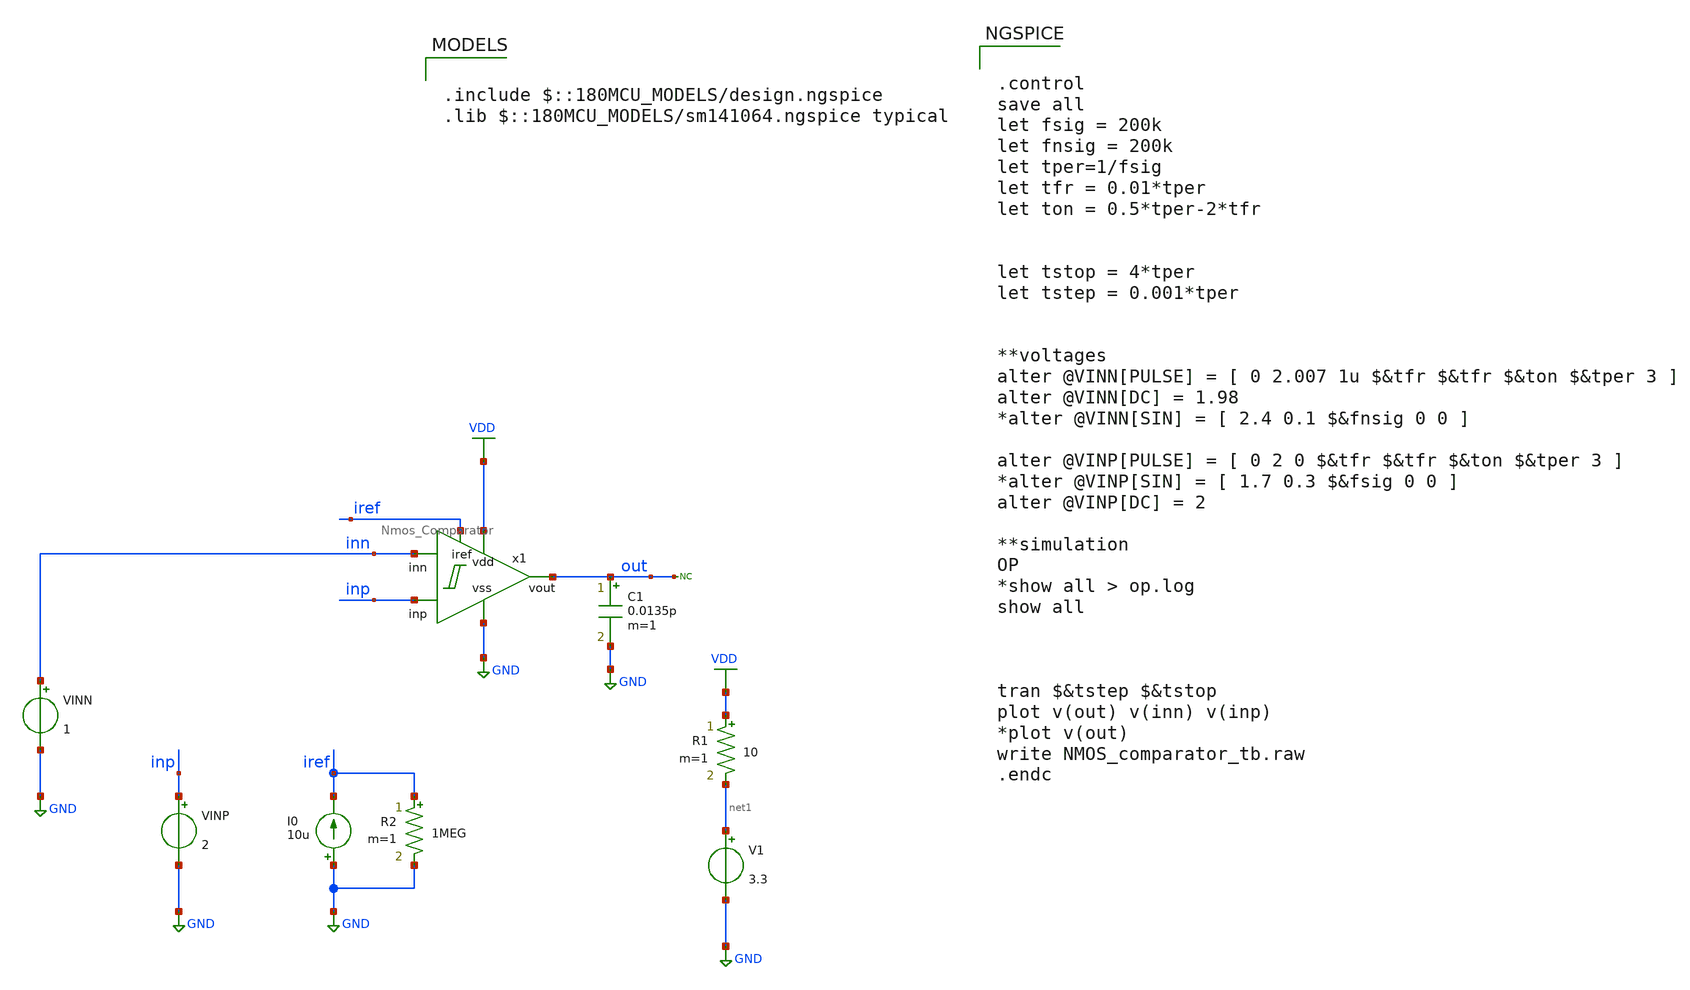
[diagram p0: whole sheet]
** sch_path: designs/libs/tb_analog/Comparator/NMOS_comparator_tb.sch
**.subckt NMOS_comparator_tb
I0 GND iref 10u
V1 net1 GND 3.3
VINP inp GND 2
* noconn out
VINN inn GND 1
x1 VDD out inp GND inn iref Nmos_Comparator
C1 out GND 0.0135p m=1
R1 VDD net1 10 m=1
R2 iref GND 1MEG m=1
**** begin user architecture code


.control
save all
let fsig = 200k
let fnsig = 200k
let tper=1/fsig
let tfr = 0.01*tper
let ton = 0.5*tper-2*tfr


let tstop = 4*tper
let tstep = 0.001*tper


**voltages
alter @VINN[PULSE] = [ 0 2.007 1u $&tfr $&tfr $&ton $&tper 3 ]
alter @VINN[DC] = 1.98
*alter @VINN[SIN] = [ 2.4 0.1 $&fnsig 0 0 ]

alter @VINP[PULSE] = [ 0 2 0 $&tfr $&tfr $&ton $&tper 3 ]
*alter @VINP[SIN] = [ 1.7 0.3 $&fsig 0 0 ]
alter @VINP[DC] = 2

**simulation
OP
*show all > op.log
show all



tran $&tstep $&tstop
plot v(out) v(inn) v(inp)
*plot v(out)
write NMOS_comparator_tb.raw
.endc



.include $::180MCU_MODELS/design.ngspice
.lib $::180MCU_MODELS/sm141064.ngspice typical

**** end user architecture code
**.ends

* expanding   symbol:  libs/core_analog/Comparator/Nmos_Comparator.sym # of pins=6
** sym_path: designs/libs/core_analog/Comparator/Nmos_Comparator.sym
** sch_path: designs/libs/core_analog/Comparator/Nmos_Comparator.sch
.subckt Nmos_Comparator vdd vout inp vss inn iref
*.ipin vss
*.ipin vdd
*.ipin iref
*.ipin inn
*.ipin inp
*.opin vout
XM3 net1 net1 vss vss nfet_03v3 L=1u W=3.5u nf=1 ad='int((nf+1)/2) * W/nf * 0.18u' as='int((nf+2)/2) * W/nf * 0.18u'
+ pd='2*int((nf+1)/2) * (W/nf + 0.18u)' ps='2*int((nf+2)/2) * (W/nf + 0.18u)' nrd='0.18u / W' nrs='0.18u / W'
+ sa=0 sb=0 sd=0 m=1
XM4 vout net1 vss vss nfet_03v3 L=1u W=3.5u nf=1 ad='int((nf+1)/2) * W/nf * 0.18u' as='int((nf+2)/2) * W/nf * 0.18u'
+ pd='2*int((nf+1)/2) * (W/nf + 0.18u)' ps='2*int((nf+2)/2) * (W/nf + 0.18u)' nrd='0.18u / W' nrs='0.18u / W'
+ sa=0 sb=0 sd=0 m=1
XM5 net2 inn net3 vss nfet_03v3 L=1u W=4u nf=1 ad='int((nf+1)/2) * W/nf * 0.18u' as='int((nf+2)/2) * W/nf * 0.18u'
+ pd='2*int((nf+1)/2) * (W/nf + 0.18u)' ps='2*int((nf+2)/2) * (W/nf + 0.18u)' nrd='0.18u / W' nrs='0.18u / W'
+ sa=0 sb=0 sd=0 m=1
XM6 net4 inp net3 vss nfet_03v3 L=1u W=4u nf=1 ad='int((nf+1)/2) * W/nf * 0.18u' as='int((nf+2)/2) * W/nf * 0.18u'
+ pd='2*int((nf+1)/2) * (W/nf + 0.18u)' ps='2*int((nf+2)/2) * (W/nf + 0.18u)' nrd='0.18u / W' nrs='0.18u / W'
+ sa=0 sb=0 sd=0 m=1
XM7 net1 net2 vdd vdd pfet_03v3 L=0.5u W=16.5u nf=4 ad='int((nf+1)/2) * W/nf * 0.18u' as='int((nf+2)/2) * W/nf * 0.18u'
+ pd='2*int((nf+1)/2) * (W/nf + 0.18u)' ps='2*int((nf+2)/2) * (W/nf + 0.18u)' nrd='0.18u / W' nrs='0.18u / W'
+ sa=0 sb=0 sd=0 m=1
XM9 net4 net4 vdd vdd pfet_03v3 L=0.5u W=10u nf=2 ad='int((nf+1)/2) * W/nf * 0.18u' as='int((nf+2)/2) * W/nf * 0.18u'
+ pd='2*int((nf+1)/2) * (W/nf + 0.18u)' ps='2*int((nf+2)/2) * (W/nf + 0.18u)' nrd='0.18u / W' nrs='0.18u / W'
+ sa=0 sb=0 sd=0 m=1
XM11 net2 net2 vdd vdd pfet_03v3 L=0.5u W=10u nf=2 ad='int((nf+1)/2) * W/nf * 0.18u' as='int((nf+2)/2) * W/nf * 0.18u'
+ pd='2*int((nf+1)/2) * (W/nf + 0.18u)' ps='2*int((nf+2)/2) * (W/nf + 0.18u)' nrd='0.18u / W' nrs='0.18u / W'
+ sa=0 sb=0 sd=0 m=1
XM12 vout net4 vdd vdd pfet_03v3 L=0.5u W=16.5u nf=4 ad='int((nf+1)/2) * W/nf * 0.18u' as='int((nf+2)/2) * W/nf * 0.18u'
+ pd='2*int((nf+1)/2) * (W/nf + 0.18u)' ps='2*int((nf+2)/2) * (W/nf + 0.18u)' nrd='0.18u / W' nrs='0.18u / W'
+ sa=0 sb=0 sd=0 m=1
XM1 net4 net2 vdd vdd pfet_03v3 L=0.5u W=10u nf=2 ad='int((nf+1)/2) * W/nf * 0.18u' as='int((nf+2)/2) * W/nf * 0.18u'
+ pd='2*int((nf+1)/2) * (W/nf + 0.18u)' ps='2*int((nf+2)/2) * (W/nf + 0.18u)' nrd='0.18u / W' nrs='0.18u / W'
+ sa=0 sb=0 sd=0 m=1
XM2 net2 net4 vdd vdd pfet_03v3 L=0.5u W=10u nf=2 ad='int((nf+1)/2) * W/nf * 0.18u' as='int((nf+2)/2) * W/nf * 0.18u'
+ pd='2*int((nf+1)/2) * (W/nf + 0.18u)' ps='2*int((nf+2)/2) * (W/nf + 0.18u)' nrd='0.18u / W' nrs='0.18u / W'
+ sa=0 sb=0 sd=0 m=1
XM8 iref iref vss vss nfet_03v3 L=1u W=2.5u nf=1 ad='int((nf+1)/2) * W/nf * 0.18u' as='int((nf+2)/2) * W/nf * 0.18u'
+ pd='2*int((nf+1)/2) * (W/nf + 0.18u)' ps='2*int((nf+2)/2) * (W/nf + 0.18u)' nrd='0.18u / W' nrs='0.18u / W'
+ sa=0 sb=0 sd=0 m=1
XM10 net3 iref vss vss nfet_03v3 L=1u W=5u nf=2 ad='int((nf+1)/2) * W/nf * 0.18u' as='int((nf+2)/2) * W/nf * 0.18u'
+ pd='2*int((nf+1)/2) * (W/nf + 0.18u)' ps='2*int((nf+2)/2) * (W/nf + 0.18u)' nrd='0.18u / W' nrs='0.18u / W'
+ sa=0 sb=0 sd=0 m=1
.ends

.GLOBAL GND
.GLOBAL VDD
.end
